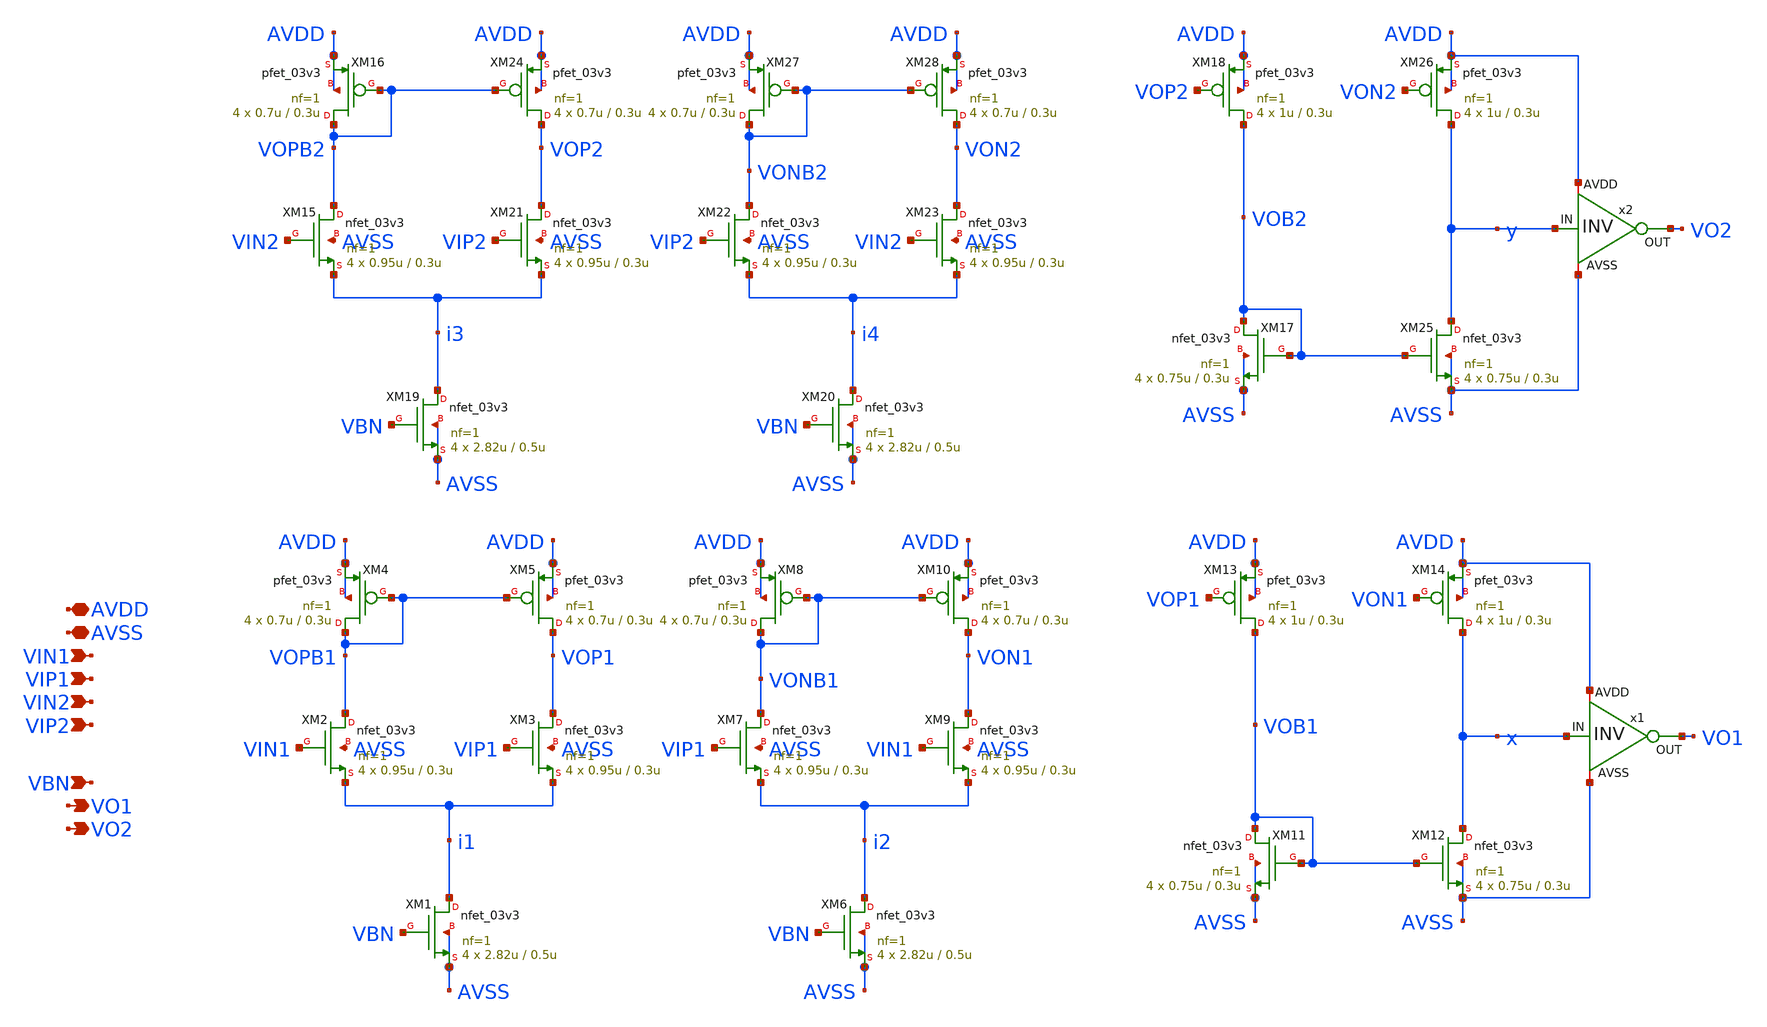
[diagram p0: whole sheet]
** sch_path: designs/libs/core_analog/d2s_converter/d2s_converter.sch
**.subckt d2s_converter AVDD AVSS VIN1 VIP1 VO1 VBN VO2 VIN2 VIP2
*.iopin AVDD
*.iopin AVSS
*.ipin VIN1
*.ipin VIP1
*.opin VO1
*.ipin VBN
*.opin VO2
*.ipin VIN2
*.ipin VIP2
XM2 VOPB1 VIN1 i1 AVSS nfet_03v3 L=0.3u W=0.95u nf=1 ad='int((nf+1)/2) * W/nf * 0.18u' as='int((nf+2)/2) * W/nf * 0.18u'
+ pd='2*int((nf+1)/2) * (W/nf + 0.18u)' ps='2*int((nf+2)/2) * (W/nf + 0.18u)' nrd='0.18u / W' nrs='0.18u / W'
+ sa=0 sb=0 sd=0 m=4
XM4 VOPB1 VOPB1 AVDD AVDD pfet_03v3 L=0.3u W=0.7u nf=1 ad='int((nf+1)/2) * W/nf * 0.18u' as='int((nf+2)/2) * W/nf * 0.18u'
+ pd='2*int((nf+1)/2) * (W/nf + 0.18u)' ps='2*int((nf+2)/2) * (W/nf + 0.18u)' nrd='0.18u / W' nrs='0.18u / W'
+ sa=0 sb=0 sd=0 m=4
XM11 VOB1 VOB1 AVSS AVSS nfet_03v3 L=0.3u W=0.75u nf=1 ad='int((nf+1)/2) * W/nf * 0.18u' as='int((nf+2)/2) * W/nf * 0.18u'
+ pd='2*int((nf+1)/2) * (W/nf + 0.18u)' ps='2*int((nf+2)/2) * (W/nf + 0.18u)' nrd='0.18u / W' nrs='0.18u / W'
+ sa=0 sb=0 sd=0 m=4
XM13 VOB1 VOP1 AVDD AVDD pfet_03v3 L=0.3u W=1u nf=1 ad='int((nf+1)/2) * W/nf * 0.18u' as='int((nf+2)/2) * W/nf * 0.18u'
+ pd='2*int((nf+1)/2) * (W/nf + 0.18u)' ps='2*int((nf+2)/2) * (W/nf + 0.18u)' nrd='0.18u / W' nrs='0.18u / W'
+ sa=0 sb=0 sd=0 m=4
XM1 i1 VBN AVSS AVSS nfet_03v3 L=0.5u W=2.82u nf=1 ad='int((nf+1)/2) * W/nf * 0.18u' as='int((nf+2)/2) * W/nf * 0.18u'
+ pd='2*int((nf+1)/2) * (W/nf + 0.18u)' ps='2*int((nf+2)/2) * (W/nf + 0.18u)' nrd='0.18u / W' nrs='0.18u / W'
+ sa=0 sb=0 sd=0 m=4
x2 AVDD y VO2 AVSS inv
x1 AVDD x VO1 AVSS inv
XM3 VOP1 VIP1 i1 AVSS nfet_03v3 L=0.3u W=0.95u nf=1 ad='int((nf+1)/2) * W/nf * 0.18u' as='int((nf+2)/2) * W/nf * 0.18u'
+ pd='2*int((nf+1)/2) * (W/nf + 0.18u)' ps='2*int((nf+2)/2) * (W/nf + 0.18u)' nrd='0.18u / W' nrs='0.18u / W'
+ sa=0 sb=0 sd=0 m=4
XM7 VONB1 VIP1 i2 AVSS nfet_03v3 L=0.3u W=0.95u nf=1 ad='int((nf+1)/2) * W/nf * 0.18u' as='int((nf+2)/2) * W/nf * 0.18u'
+ pd='2*int((nf+1)/2) * (W/nf + 0.18u)' ps='2*int((nf+2)/2) * (W/nf + 0.18u)' nrd='0.18u / W' nrs='0.18u / W'
+ sa=0 sb=0 sd=0 m=4
XM9 VON1 VIN1 i2 AVSS nfet_03v3 L=0.3u W=0.95u nf=1 ad='int((nf+1)/2) * W/nf * 0.18u' as='int((nf+2)/2) * W/nf * 0.18u'
+ pd='2*int((nf+1)/2) * (W/nf + 0.18u)' ps='2*int((nf+2)/2) * (W/nf + 0.18u)' nrd='0.18u / W' nrs='0.18u / W'
+ sa=0 sb=0 sd=0 m=4
XM5 VOP1 VOPB1 AVDD AVDD pfet_03v3 L=0.3u W=0.7u nf=1 ad='int((nf+1)/2) * W/nf * 0.18u' as='int((nf+2)/2) * W/nf * 0.18u'
+ pd='2*int((nf+1)/2) * (W/nf + 0.18u)' ps='2*int((nf+2)/2) * (W/nf + 0.18u)' nrd='0.18u / W' nrs='0.18u / W'
+ sa=0 sb=0 sd=0 m=4
XM8 VONB1 VONB1 AVDD AVDD pfet_03v3 L=0.3u W=0.7u nf=1 ad='int((nf+1)/2) * W/nf * 0.18u' as='int((nf+2)/2) * W/nf * 0.18u'
+ pd='2*int((nf+1)/2) * (W/nf + 0.18u)' ps='2*int((nf+2)/2) * (W/nf + 0.18u)' nrd='0.18u / W' nrs='0.18u / W'
+ sa=0 sb=0 sd=0 m=4
XM10 VON1 VONB1 AVDD AVDD pfet_03v3 L=0.3u W=0.7u nf=1 ad='int((nf+1)/2) * W/nf * 0.18u' as='int((nf+2)/2) * W/nf * 0.18u'
+ pd='2*int((nf+1)/2) * (W/nf + 0.18u)' ps='2*int((nf+2)/2) * (W/nf + 0.18u)' nrd='0.18u / W' nrs='0.18u / W'
+ sa=0 sb=0 sd=0 m=4
XM15 VOPB2 VIN2 i3 AVSS nfet_03v3 L=0.3u W=0.95u nf=1 ad='int((nf+1)/2) * W/nf * 0.18u' as='int((nf+2)/2) * W/nf * 0.18u'
+ pd='2*int((nf+1)/2) * (W/nf + 0.18u)' ps='2*int((nf+2)/2) * (W/nf + 0.18u)' nrd='0.18u / W' nrs='0.18u / W'
+ sa=0 sb=0 sd=0 m=4
XM16 VOPB2 VOPB2 AVDD AVDD pfet_03v3 L=0.3u W=0.7u nf=1 ad='int((nf+1)/2) * W/nf * 0.18u' as='int((nf+2)/2) * W/nf * 0.18u'
+ pd='2*int((nf+1)/2) * (W/nf + 0.18u)' ps='2*int((nf+2)/2) * (W/nf + 0.18u)' nrd='0.18u / W' nrs='0.18u / W'
+ sa=0 sb=0 sd=0 m=4
XM21 VOP2 VIP2 i3 AVSS nfet_03v3 L=0.3u W=0.95u nf=1 ad='int((nf+1)/2) * W/nf * 0.18u' as='int((nf+2)/2) * W/nf * 0.18u'
+ pd='2*int((nf+1)/2) * (W/nf + 0.18u)' ps='2*int((nf+2)/2) * (W/nf + 0.18u)' nrd='0.18u / W' nrs='0.18u / W'
+ sa=0 sb=0 sd=0 m=4
XM22 VONB2 VIP2 i4 AVSS nfet_03v3 L=0.3u W=0.95u nf=1 ad='int((nf+1)/2) * W/nf * 0.18u' as='int((nf+2)/2) * W/nf * 0.18u'
+ pd='2*int((nf+1)/2) * (W/nf + 0.18u)' ps='2*int((nf+2)/2) * (W/nf + 0.18u)' nrd='0.18u / W' nrs='0.18u / W'
+ sa=0 sb=0 sd=0 m=4
XM23 VON2 VIN2 i4 AVSS nfet_03v3 L=0.3u W=0.95u nf=1 ad='int((nf+1)/2) * W/nf * 0.18u' as='int((nf+2)/2) * W/nf * 0.18u'
+ pd='2*int((nf+1)/2) * (W/nf + 0.18u)' ps='2*int((nf+2)/2) * (W/nf + 0.18u)' nrd='0.18u / W' nrs='0.18u / W'
+ sa=0 sb=0 sd=0 m=4
XM24 VOP2 VOPB2 AVDD AVDD pfet_03v3 L=0.3u W=0.7u nf=1 ad='int((nf+1)/2) * W/nf * 0.18u' as='int((nf+2)/2) * W/nf * 0.18u'
+ pd='2*int((nf+1)/2) * (W/nf + 0.18u)' ps='2*int((nf+2)/2) * (W/nf + 0.18u)' nrd='0.18u / W' nrs='0.18u / W'
+ sa=0 sb=0 sd=0 m=4
XM27 VONB2 VONB2 AVDD AVDD pfet_03v3 L=0.3u W=0.7u nf=1 ad='int((nf+1)/2) * W/nf * 0.18u' as='int((nf+2)/2) * W/nf * 0.18u'
+ pd='2*int((nf+1)/2) * (W/nf + 0.18u)' ps='2*int((nf+2)/2) * (W/nf + 0.18u)' nrd='0.18u / W' nrs='0.18u / W'
+ sa=0 sb=0 sd=0 m=4
XM28 VON2 VONB2 AVDD AVDD pfet_03v3 L=0.3u W=0.7u nf=1 ad='int((nf+1)/2) * W/nf * 0.18u' as='int((nf+2)/2) * W/nf * 0.18u'
+ pd='2*int((nf+1)/2) * (W/nf + 0.18u)' ps='2*int((nf+2)/2) * (W/nf + 0.18u)' nrd='0.18u / W' nrs='0.18u / W'
+ sa=0 sb=0 sd=0 m=4
XM12 x VOB1 AVSS AVSS nfet_03v3 L=0.3u W=0.75u nf=1 ad='int((nf+1)/2) * W/nf * 0.18u' as='int((nf+2)/2) * W/nf * 0.18u'
+ pd='2*int((nf+1)/2) * (W/nf + 0.18u)' ps='2*int((nf+2)/2) * (W/nf + 0.18u)' nrd='0.18u / W' nrs='0.18u / W'
+ sa=0 sb=0 sd=0 m=4
XM14 x VON1 AVDD AVDD pfet_03v3 L=0.3u W=1u nf=1 ad='int((nf+1)/2) * W/nf * 0.18u' as='int((nf+2)/2) * W/nf * 0.18u'
+ pd='2*int((nf+1)/2) * (W/nf + 0.18u)' ps='2*int((nf+2)/2) * (W/nf + 0.18u)' nrd='0.18u / W' nrs='0.18u / W'
+ sa=0 sb=0 sd=0 m=4
XM17 VOB2 VOB2 AVSS AVSS nfet_03v3 L=0.3u W=0.75u nf=1 ad='int((nf+1)/2) * W/nf * 0.18u' as='int((nf+2)/2) * W/nf * 0.18u'
+ pd='2*int((nf+1)/2) * (W/nf + 0.18u)' ps='2*int((nf+2)/2) * (W/nf + 0.18u)' nrd='0.18u / W' nrs='0.18u / W'
+ sa=0 sb=0 sd=0 m=4
XM18 VOB2 VOP2 AVDD AVDD pfet_03v3 L=0.3u W=1u nf=1 ad='int((nf+1)/2) * W/nf * 0.18u' as='int((nf+2)/2) * W/nf * 0.18u'
+ pd='2*int((nf+1)/2) * (W/nf + 0.18u)' ps='2*int((nf+2)/2) * (W/nf + 0.18u)' nrd='0.18u / W' nrs='0.18u / W'
+ sa=0 sb=0 sd=0 m=4
XM25 y VOB2 AVSS AVSS nfet_03v3 L=0.3u W=0.75u nf=1 ad='int((nf+1)/2) * W/nf * 0.18u' as='int((nf+2)/2) * W/nf * 0.18u'
+ pd='2*int((nf+1)/2) * (W/nf + 0.18u)' ps='2*int((nf+2)/2) * (W/nf + 0.18u)' nrd='0.18u / W' nrs='0.18u / W'
+ sa=0 sb=0 sd=0 m=4
XM26 y VON2 AVDD AVDD pfet_03v3 L=0.3u W=1u nf=1 ad='int((nf+1)/2) * W/nf * 0.18u' as='int((nf+2)/2) * W/nf * 0.18u'
+ pd='2*int((nf+1)/2) * (W/nf + 0.18u)' ps='2*int((nf+2)/2) * (W/nf + 0.18u)' nrd='0.18u / W' nrs='0.18u / W'
+ sa=0 sb=0 sd=0 m=4
XM6 i2 VBN AVSS AVSS nfet_03v3 L=0.5u W=2.82u nf=1 ad='int((nf+1)/2) * W/nf * 0.18u' as='int((nf+2)/2) * W/nf * 0.18u'
+ pd='2*int((nf+1)/2) * (W/nf + 0.18u)' ps='2*int((nf+2)/2) * (W/nf + 0.18u)' nrd='0.18u / W' nrs='0.18u / W'
+ sa=0 sb=0 sd=0 m=4
XM19 i3 VBN AVSS AVSS nfet_03v3 L=0.5u W=2.82u nf=1 ad='int((nf+1)/2) * W/nf * 0.18u' as='int((nf+2)/2) * W/nf * 0.18u'
+ pd='2*int((nf+1)/2) * (W/nf + 0.18u)' ps='2*int((nf+2)/2) * (W/nf + 0.18u)' nrd='0.18u / W' nrs='0.18u / W'
+ sa=0 sb=0 sd=0 m=4
XM20 i4 VBN AVSS AVSS nfet_03v3 L=0.5u W=2.82u nf=1 ad='int((nf+1)/2) * W/nf * 0.18u' as='int((nf+2)/2) * W/nf * 0.18u'
+ pd='2*int((nf+1)/2) * (W/nf + 0.18u)' ps='2*int((nf+2)/2) * (W/nf + 0.18u)' nrd='0.18u / W' nrs='0.18u / W'
+ sa=0 sb=0 sd=0 m=4
**.ends

* expanding   symbol:  libs/core_analog/inv/inv.sym # of pins=4
** sym_path: designs/libs/core_analog/inv/inv.sym
** sch_path: designs/libs/core_analog/inv/inv.sch
.subckt inv AVDD IN OUT AVSS
*.ipin IN
*.iopin AVDD
*.iopin AVSS
*.opin OUT
XM1 OUT IN AVDD AVDD pfet_03v3 L=0.28u W=0.9u nf=1 ad='int((nf+1)/2) * W/nf * 0.18u' as='int((nf+2)/2) * W/nf * 0.18u'
+ pd='2*int((nf+1)/2) * (W/nf + 0.18u)' ps='2*int((nf+2)/2) * (W/nf + 0.18u)' nrd='0.18u / W' nrs='0.18u / W'
+ sa=0 sb=0 sd=0 m=1
XM2 OUT IN AVSS AVSS nfet_03v3 L=0.28u W=0.3u nf=1 ad='int((nf+1)/2) * W/nf * 0.18u' as='int((nf+2)/2) * W/nf * 0.18u'
+ pd='2*int((nf+1)/2) * (W/nf + 0.18u)' ps='2*int((nf+2)/2) * (W/nf + 0.18u)' nrd='0.18u / W' nrs='0.18u / W'
+ sa=0 sb=0 sd=0 m=1
.ends

.end
